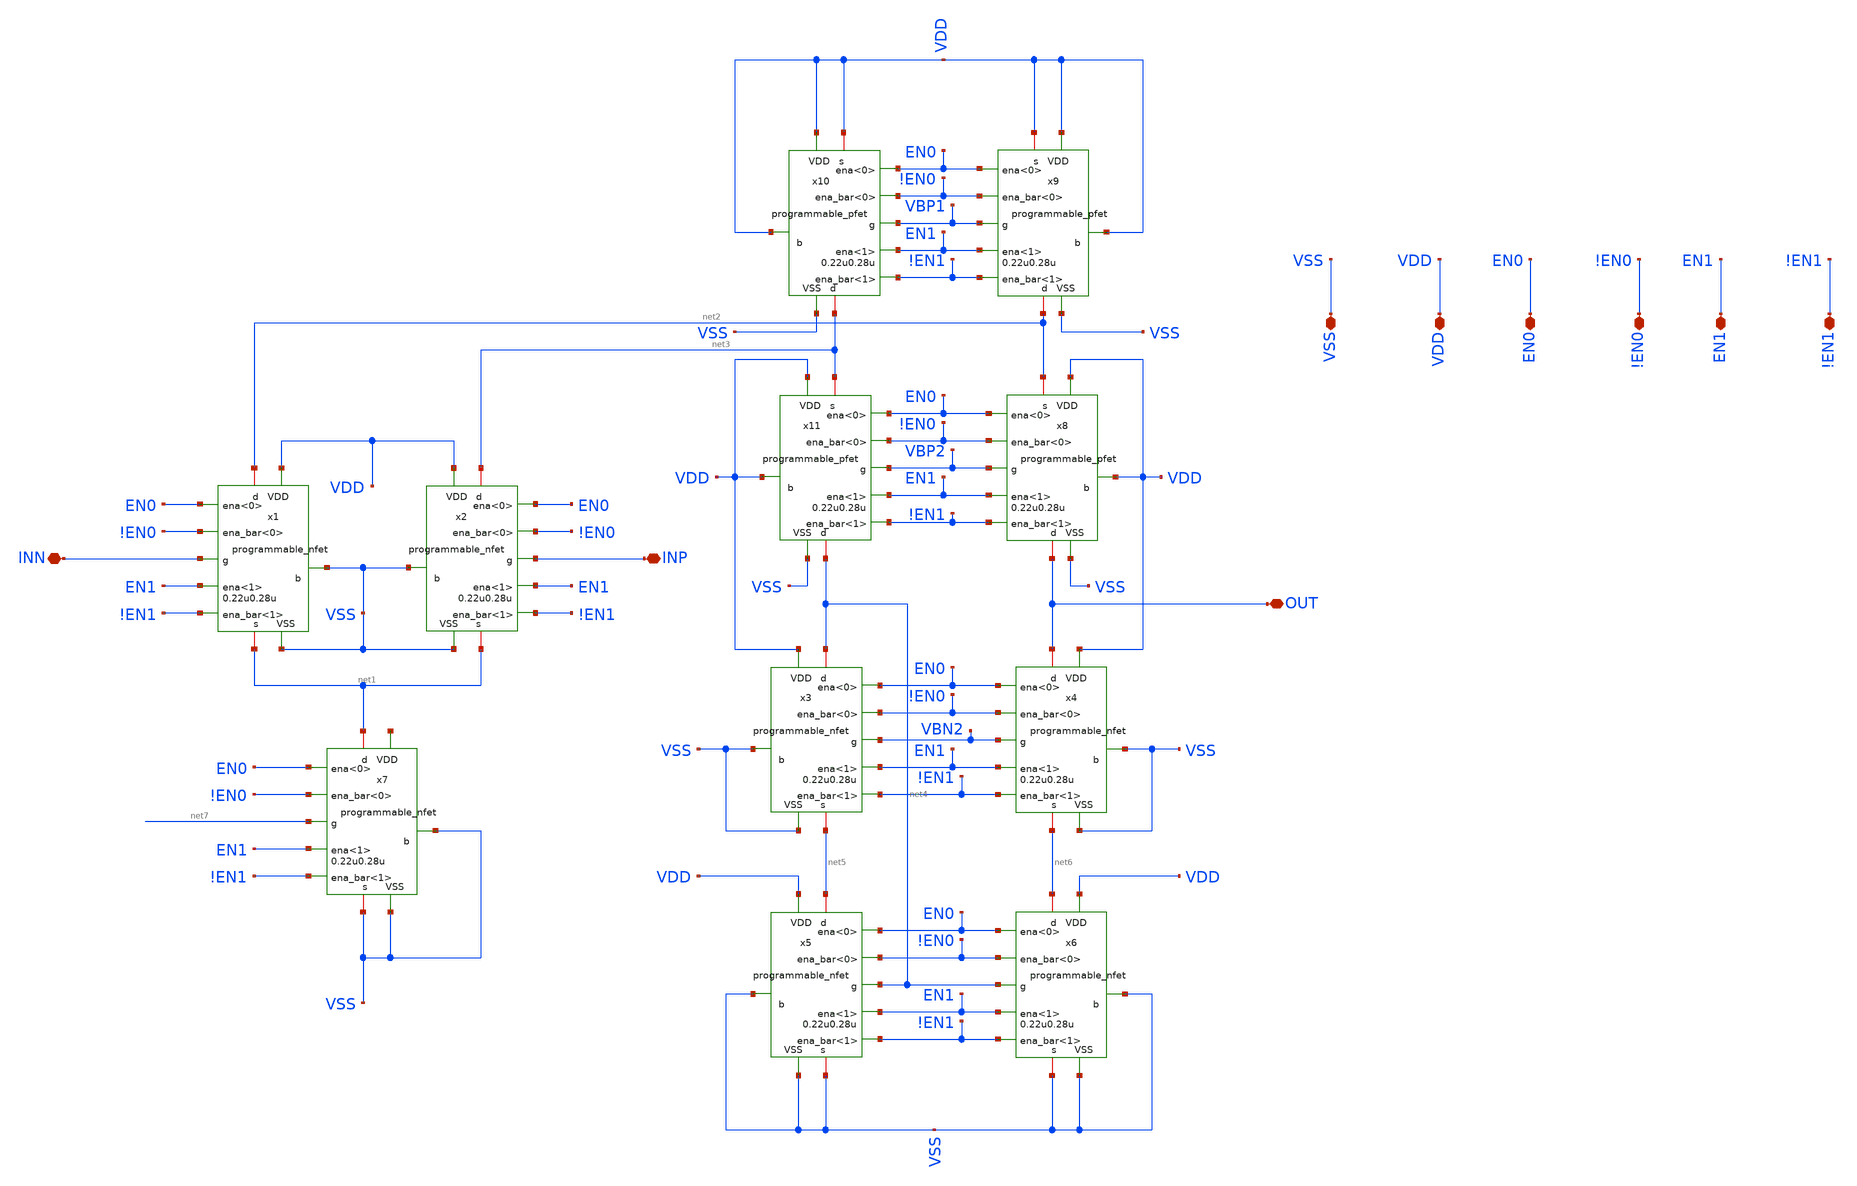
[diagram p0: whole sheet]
** sch_path: designs/libs/core_amps/ota_folded_cascode/programmable_folded.sch
**.subckt programmable_folded OUT VSS VDD EN0 !EN0 EN1 !EN1 INN INP
*.iopin OUT
*.iopin VSS
*.iopin VDD
*.iopin EN0
*.iopin !EN0
*.iopin EN1
*.iopin !EN1
*.iopin INN
*.iopin INP
x1 net2 VSS INN net1 !EN0 VDD !EN1 EN0 EN1 VSS programmable_nfet width=0.22u length=0.28u
x2 net3 VSS INP net1 !EN0 VDD !EN1 EN0 EN1 VSS programmable_nfet width=0.22u length=0.28u
x3 net4 VSS VBN2 net5 !EN0 VDD !EN1 EN0 EN1 VSS programmable_nfet width=0.22u length=0.28u
x4 OUT VSS VBN2 net6 !EN0 VDD !EN1 EN0 EN1 VSS programmable_nfet width=0.22u length=0.28u
x5 net5 VSS net4 VSS !EN0 VDD !EN1 EN0 EN1 VSS programmable_nfet width=0.22u length=0.28u
x6 net6 VSS net4 VSS !EN0 VDD !EN1 EN0 EN1 VSS programmable_nfet width=0.22u length=0.28u
x7 net1 VSS net7 VSS !EN0 net8 !EN1 EN0 EN1 VSS programmable_nfet width=0.22u length=0.28u
x8 OUT VDD VBP2 net2 !EN0 VDD !EN1 EN0 EN1 VSS programmable_pfet width=0.22u length=0.28u
x9 net2 VDD VBP1 VDD !EN0 VDD !EN1 EN0 EN1 VSS programmable_pfet width=0.22u length=0.28u
x10 net3 VDD VBP1 VDD !EN0 VDD !EN1 EN0 EN1 VSS programmable_pfet width=0.22u length=0.28u
x11 net4 VDD VBP2 net3 !EN0 VDD !EN1 EN0 EN1 VSS programmable_pfet width=0.22u length=0.28u
**.ends
.end
